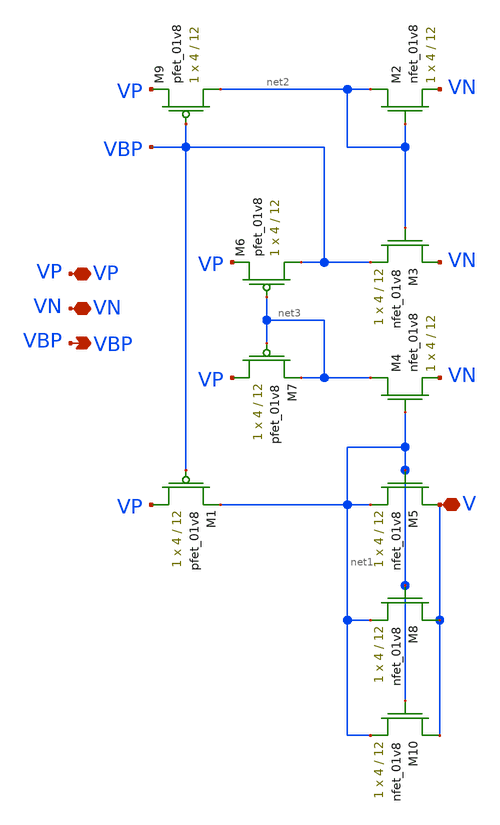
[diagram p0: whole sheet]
** sch_path: dac/layout/bias_gen/bias_gen_layout.sch
**.subckt bias_gen_layout VN VP VBP V
*.iopin VN
*.iopin VP
*.opin VBP
*.iopin V
XM5 V net1 net1 VN sky130_fd_pr__nfet_01v8 L=12 W=4 nf=1 ad='int((nf+1)/2) * W/nf * 0.29' as='int((nf+2)/2) * W/nf * 0.29'
+ pd='2*int((nf+1)/2) * (W/nf + 0.29)' ps='2*int((nf+2)/2) * (W/nf + 0.29)' nrd='0.29 / W' nrs='0.29 / W'
+ sa=0 sb=0 sd=0 mult=1 m=1
XM2 net2 net2 VN VN sky130_fd_pr__nfet_01v8 L=12 W=4 nf=1 ad='int((nf+1)/2) * W/nf * 0.29' as='int((nf+2)/2) * W/nf * 0.29'
+ pd='2*int((nf+1)/2) * (W/nf + 0.29)' ps='2*int((nf+2)/2) * (W/nf + 0.29)' nrd='0.29 / W' nrs='0.29 / W'
+ sa=0 sb=0 sd=0 mult=1 m=1
XM9 net2 VBP VP VP sky130_fd_pr__pfet_01v8 L=12 W=4 nf=1 ad='int((nf+1)/2) * W/nf * 0.29' as='int((nf+2)/2) * W/nf * 0.29'
+ pd='2*int((nf+1)/2) * (W/nf + 0.29)' ps='2*int((nf+2)/2) * (W/nf + 0.29)' nrd='0.29 / W' nrs='0.29 / W'
+ sa=0 sb=0 sd=0 mult=1 m=1
XM1 VP VBP net1 VP sky130_fd_pr__pfet_01v8 L=12 W=4 nf=1 ad='int((nf+1)/2) * W/nf * 0.29' as='int((nf+2)/2) * W/nf * 0.29'
+ pd='2*int((nf+1)/2) * (W/nf + 0.29)' ps='2*int((nf+2)/2) * (W/nf + 0.29)' nrd='0.29 / W' nrs='0.29 / W'
+ sa=0 sb=0 sd=0 mult=1 m=1
XM3 VN net2 VBP VN sky130_fd_pr__nfet_01v8 L=12 W=4 nf=1 ad='int((nf+1)/2) * W/nf * 0.29' as='int((nf+2)/2) * W/nf * 0.29'
+ pd='2*int((nf+1)/2) * (W/nf + 0.29)' ps='2*int((nf+2)/2) * (W/nf + 0.29)' nrd='0.29 / W' nrs='0.29 / W'
+ sa=0 sb=0 sd=0 mult=1 m=1
XM4 net3 net1 VN VN sky130_fd_pr__nfet_01v8 L=12 W=4 nf=1 ad='int((nf+1)/2) * W/nf * 0.29' as='int((nf+2)/2) * W/nf * 0.29'
+ pd='2*int((nf+1)/2) * (W/nf + 0.29)' ps='2*int((nf+2)/2) * (W/nf + 0.29)' nrd='0.29 / W' nrs='0.29 / W'
+ sa=0 sb=0 sd=0 mult=1 m=1
XM6 VBP net3 VP VP sky130_fd_pr__pfet_01v8 L=12 W=4 nf=1 ad='int((nf+1)/2) * W/nf * 0.29' as='int((nf+2)/2) * W/nf * 0.29'
+ pd='2*int((nf+1)/2) * (W/nf + 0.29)' ps='2*int((nf+2)/2) * (W/nf + 0.29)' nrd='0.29 / W' nrs='0.29 / W'
+ sa=0 sb=0 sd=0 mult=1 m=1
XM7 VP net3 net3 VP sky130_fd_pr__pfet_01v8 L=12 W=4 nf=1 ad='int((nf+1)/2) * W/nf * 0.29' as='int((nf+2)/2) * W/nf * 0.29'
+ pd='2*int((nf+1)/2) * (W/nf + 0.29)' ps='2*int((nf+2)/2) * (W/nf + 0.29)' nrd='0.29 / W' nrs='0.29 / W'
+ sa=0 sb=0 sd=0 mult=1 m=1
XM8 V net1 net1 VN sky130_fd_pr__nfet_01v8 L=12 W=4 nf=1 ad='int((nf+1)/2) * W/nf * 0.29' as='int((nf+2)/2) * W/nf * 0.29'
+ pd='2*int((nf+1)/2) * (W/nf + 0.29)' ps='2*int((nf+2)/2) * (W/nf + 0.29)' nrd='0.29 / W' nrs='0.29 / W'
+ sa=0 sb=0 sd=0 mult=1 m=1
XM10 V net1 net1 VN sky130_fd_pr__nfet_01v8 L=12 W=4 nf=1 ad='int((nf+1)/2) * W/nf * 0.29' as='int((nf+2)/2) * W/nf * 0.29'
+ pd='2*int((nf+1)/2) * (W/nf + 0.29)' ps='2*int((nf+2)/2) * (W/nf + 0.29)' nrd='0.29 / W' nrs='0.29 / W'
+ sa=0 sb=0 sd=0 mult=1 m=1
**.ends
.end
